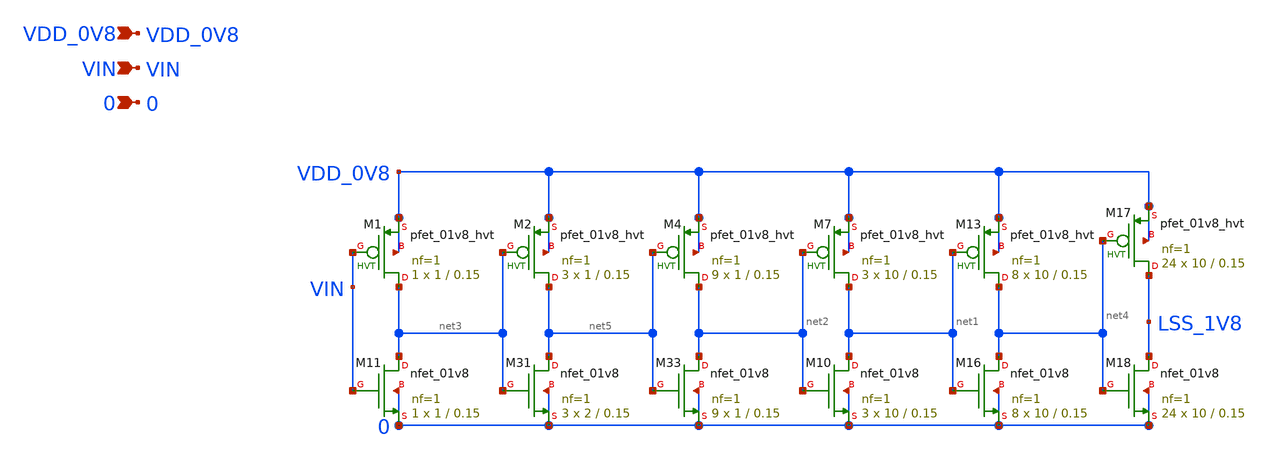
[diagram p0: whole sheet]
** sch_path: design/LELO_SVOD_SKY130A/LELO_SVOD_TRANSITOR_TEST.sch
**.subckt LELO_SVOD_TRANSITOR_TEST VDD_0V8 0 VIN
*.ipin VDD_0V8
*.ipin 0
*.ipin VIN
XM11 net3 VIN 0 0 sky130_fd_pr__nfet_01v8 L=0.15 W=1 nf=1 ad='int((1 + 1)/2) * 1 / 1 * 0.29' as='int((1 + 2)/2) * 1 / 1 * 0.29'
+ pd='2*int((1 + 1)/2) * (1 / 1 + 0.29)' ps='2*int((1 + 2)/2) * (1 / 1 + 0.29)' nrd='0.29 / 1 ' nrs='0.29 / 1 '
+ sa=0 sb=0 sd=0 mult=1 m=1
XM31 net5 net3 0 0 sky130_fd_pr__nfet_01v8 L=0.15 W=2 nf=1 ad='int((1 + 1)/2) * 2 / 1 * 0.29' as='int((1 + 2)/2) * 2 / 1 * 0.29'
+ pd='2*int((1 + 1)/2) * (2 / 1 + 0.29)' ps='2*int((1 + 2)/2) * (2 / 1 + 0.29)' nrd='0.29 / 2 ' nrs='0.29 / 2 '
+ sa=0 sb=0 sd=0 mult=3 m=3
XM33 net2 net5 0 0 sky130_fd_pr__nfet_01v8 L=0.15 W=1 nf=1 ad='int((1 + 1)/2) * 1 / 1 * 0.29' as='int((1 + 2)/2) * 1 / 1 * 0.29'
+ pd='2*int((1 + 1)/2) * (1 / 1 + 0.29)' ps='2*int((1 + 2)/2) * (1 / 1 + 0.29)' nrd='0.29 / 1 ' nrs='0.29 / 1 '
+ sa=0 sb=0 sd=0 mult=9 m=9
XM1 net3 VIN VDD_0V8 VDD_0V8 sky130_fd_pr__pfet_01v8_hvt L=0.15 W=1 nf=1 ad='int((1 + 1)/2) * 1 / 1 * 0.29'
+ as='int((1 + 2)/2) * 1 / 1 * 0.29' pd='2*int((1 + 1)/2) * (1 / 1 + 0.29)' ps='2*int((1 + 2)/2) * (1 / 1 + 0.29)'
+ nrd='0.29 / 1 ' nrs='0.29 / 1 ' sa=0 sb=0 sd=0 mult=1 m=1
XM2 net5 net3 VDD_0V8 VDD_0V8 sky130_fd_pr__pfet_01v8_hvt L=0.15 W=1 nf=1 ad='int((1 + 1)/2) * 1 / 1 * 0.29'
+ as='int((1 + 2)/2) * 1 / 1 * 0.29' pd='2*int((1 + 1)/2) * (1 / 1 + 0.29)' ps='2*int((1 + 2)/2) * (1 / 1 + 0.29)'
+ nrd='0.29 / 1 ' nrs='0.29 / 1 ' sa=0 sb=0 sd=0 mult=3 m=3
XM4 net2 net5 VDD_0V8 VDD_0V8 sky130_fd_pr__pfet_01v8_hvt L=0.15 W=1 nf=1 ad='int((1 + 1)/2) * 1 / 1 * 0.29'
+ as='int((1 + 2)/2) * 1 / 1 * 0.29' pd='2*int((1 + 1)/2) * (1 / 1 + 0.29)' ps='2*int((1 + 2)/2) * (1 / 1 + 0.29)'
+ nrd='0.29 / 1 ' nrs='0.29 / 1 ' sa=0 sb=0 sd=0 mult=9 m=9
XM7 net1 net2 VDD_0V8 VDD_0V8 sky130_fd_pr__pfet_01v8_hvt L=0.15 W=10 nf=1 ad='int((1 + 1)/2) * 10 / 1 * 0.29'
+ as='int((1 + 2)/2) * 10 / 1 * 0.29' pd='2*int((1 + 1)/2) * (10 / 1 + 0.29)' ps='2*int((1 + 2)/2) * (10 / 1 + 0.29)'
+ nrd='0.29 / 10 ' nrs='0.29 / 10 ' sa=0 sb=0 sd=0 mult=3 m=3
XM10 net1 net2 0 0 sky130_fd_pr__nfet_01v8 L=0.15 W=10 nf=1 ad='int((1 + 1)/2) * 10 / 1 * 0.29' as='int((1 + 2)/2) * 10 / 1 * 0.29'
+ pd='2*int((1 + 1)/2) * (10 / 1 + 0.29)' ps='2*int((1 + 2)/2) * (10 / 1 + 0.29)' nrd='0.29 / 10 ' nrs='0.29 / 10 '
+ sa=0 sb=0 sd=0 mult=3 m=3
XM13 net4 net1 VDD_0V8 VDD_0V8 sky130_fd_pr__pfet_01v8_hvt L=0.15 W=10 nf=1 ad='int((1 + 1)/2) * 10 / 1 * 0.29'
+ as='int((1 + 2)/2) * 10 / 1 * 0.29' pd='2*int((1 + 1)/2) * (10 / 1 + 0.29)' ps='2*int((1 + 2)/2) * (10 / 1 + 0.29)'
+ nrd='0.29 / 10 ' nrs='0.29 / 10 ' sa=0 sb=0 sd=0 mult=8 m=8
XM16 net4 net1 0 0 sky130_fd_pr__nfet_01v8 L=0.15 W=10 nf=1 ad='int((1 + 1)/2) * 10 / 1 * 0.29' as='int((1 + 2)/2) * 10 / 1 * 0.29'
+ pd='2*int((1 + 1)/2) * (10 / 1 + 0.29)' ps='2*int((1 + 2)/2) * (10 / 1 + 0.29)' nrd='0.29 / 10 ' nrs='0.29 / 10 '
+ sa=0 sb=0 sd=0 mult=8 m=8
XM17 LSS_1V8 net4 VDD_0V8 VDD_0V8 sky130_fd_pr__pfet_01v8_hvt L=0.15 W=10 nf=1 ad='int((1 + 1)/2) * 10 / 1 * 0.29'
+ as='int((1 + 2)/2) * 10 / 1 * 0.29' pd='2*int((1 + 1)/2) * (10 / 1 + 0.29)' ps='2*int((1 + 2)/2) * (10 / 1 + 0.29)'
+ nrd='0.29 / 10 ' nrs='0.29 / 10 ' sa=0 sb=0 sd=0 mult=24 m=24
XM18 LSS_1V8 net4 0 0 sky130_fd_pr__nfet_01v8 L=0.15 W=10 nf=1 ad='int((1 + 1)/2) * 10 / 1 * 0.29' as='int((1 + 2)/2) * 10 / 1 * 0.29'
+ pd='2*int((1 + 1)/2) * (10 / 1 + 0.29)' ps='2*int((1 + 2)/2) * (10 / 1 + 0.29)' nrd='0.29 / 10 ' nrs='0.29 / 10 '
+ sa=0 sb=0 sd=0 mult=24 m=24
**.ends
.end
